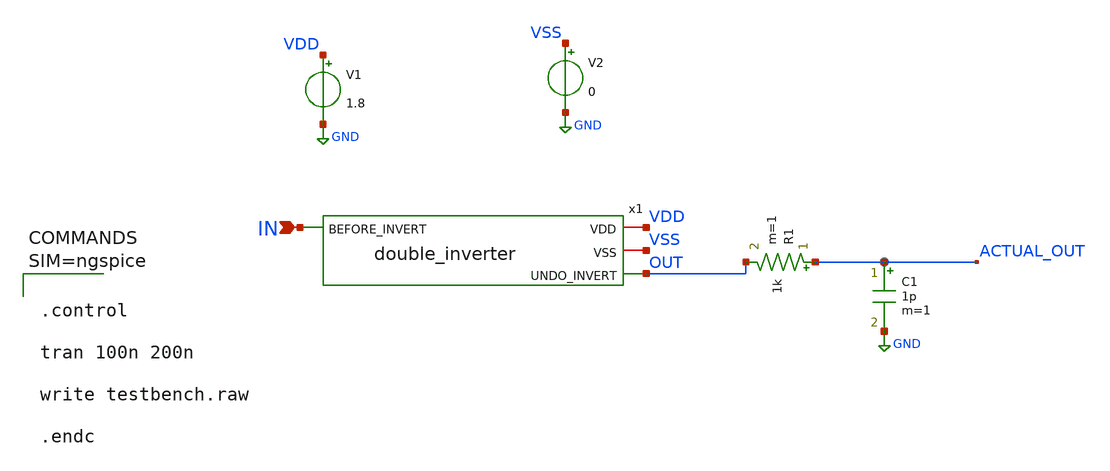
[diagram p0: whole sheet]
** sch_path: xschem/attic/testbench.sch
**.subckt testbench IN
*.ipin IN
x1 VDD VSS IN OUT double_inverter
V1 VDD GND 1.8
V2 VSS GND 0
R1 ACTUAL_OUT OUT 1k m=1
C1 ACTUAL_OUT GND 1p m=1
**** begin user architecture code

** opencircuitdesign pdks install
.lib $::SKYWATER_MODELS/sky130.lib.spice tt





.control

tran 100n 200n

write testbench.raw

.endc



**** end user architecture code
**.ends
.GLOBAL GND
.end
